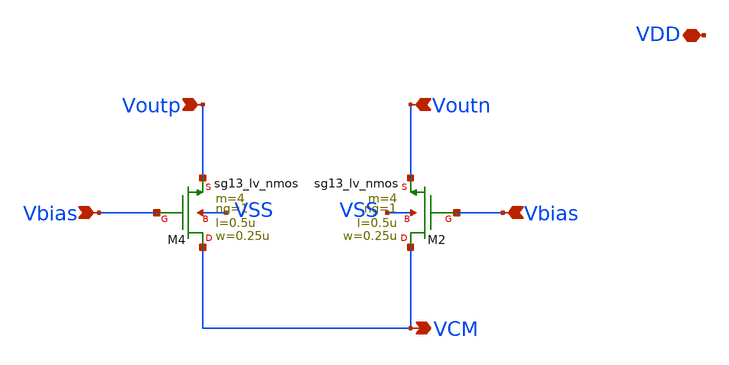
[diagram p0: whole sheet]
** sch_path: schema/ota_cmfb_cm_sense/ota_cmfb_cm_sense_shifted.sch
**.subckt ota_cmfb_cm_sense_shifted Voutp Voutn VDD VCM
*.ipin Voutp
*.ipin Voutn
*.iopin VDD
*.opin VCM
XM2 VCM Vbias Voutn VSS sg13_lv_nmos w=0.25u l=0.5u ng=1 m=4 mm_ok=1
XM4 VCM Vbias Voutp VSS sg13_lv_nmos w=0.25u l=0.5u ng=1 m=4 mm_ok=1
**.ends
.end
